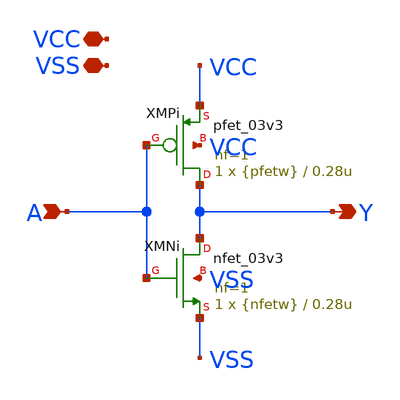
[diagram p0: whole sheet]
** sch_path: xschem/inv_param.sch
**.subckt inv_param VCC VSS A Y
*.iopin VCC
*.iopin VSS
*.ipin A
*.opin Y
XMNi Y A VSS VSS nfet_03v3 L=0.28u W={nfetw} nf=1 ad='int((nf+1)/2) * W/nf * 0.18u' as='int((nf+2)/2) * W/nf * 0.18u'
+ pd='2*int((nf+1)/2) * (W/nf + 0.18u)' ps='2*int((nf+2)/2) * (W/nf + 0.18u)' nrd='0.18u / W' nrs='0.18u / W'
+ sa=0 sb=0 sd=0 m=1
XMPi Y A VCC VCC pfet_03v3 L=0.28u W={pfetw} nf=1 ad='int((nf+1)/2) * W/nf * 0.18u' as='int((nf+2)/2) * W/nf * 0.18u'
+ pd='2*int((nf+1)/2) * (W/nf + 0.18u)' ps='2*int((nf+2)/2) * (W/nf + 0.18u)' nrd='0.18u / W' nrs='0.18u / W'
+ sa=0 sb=0 sd=0 m=1
**.ends
.end
